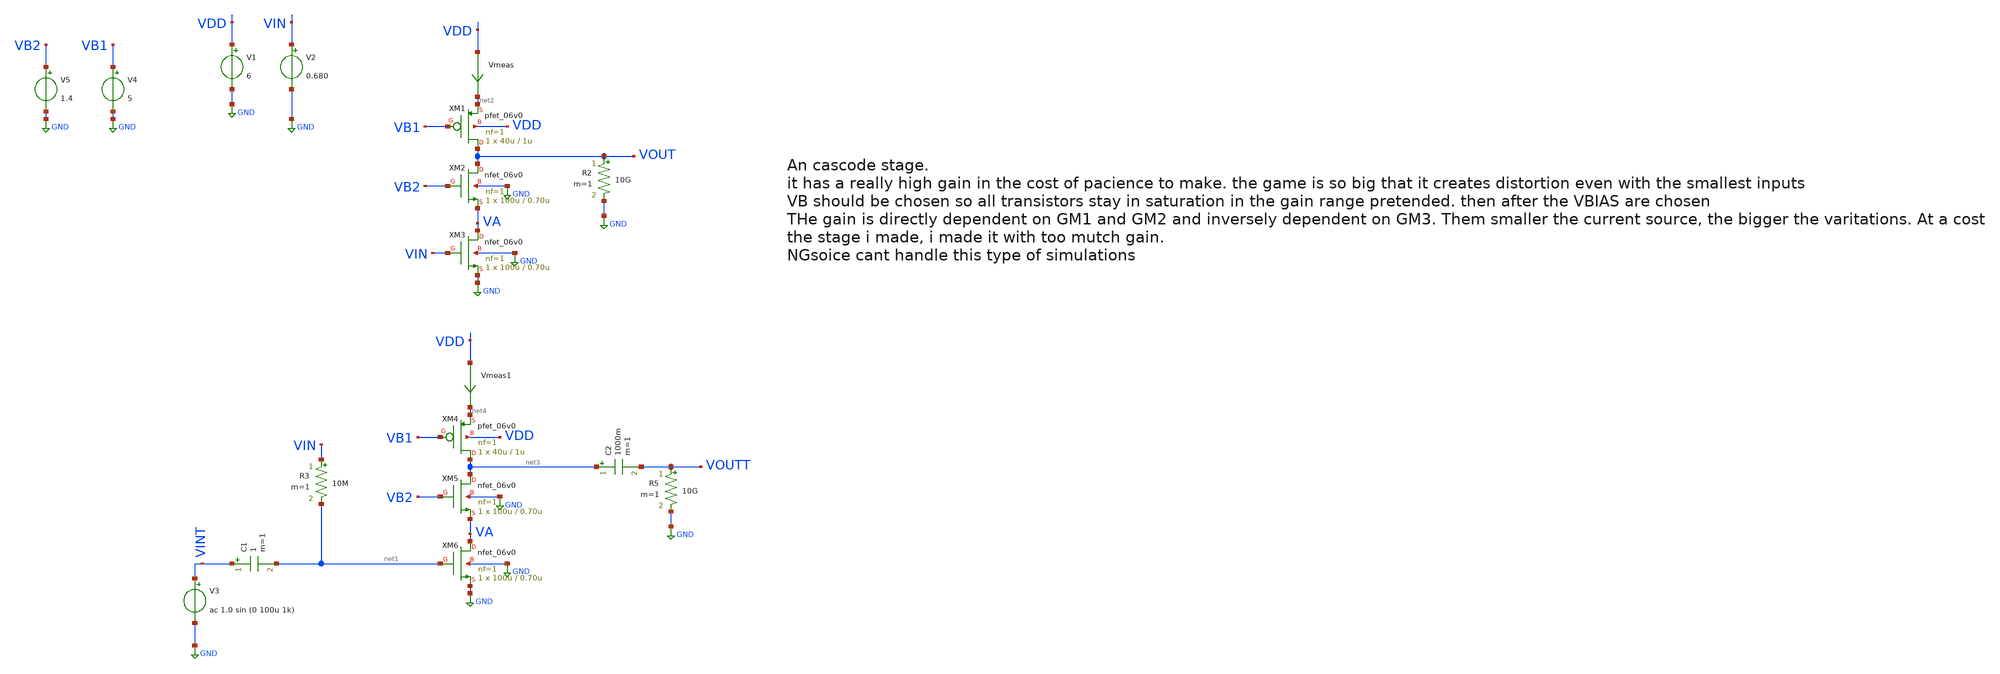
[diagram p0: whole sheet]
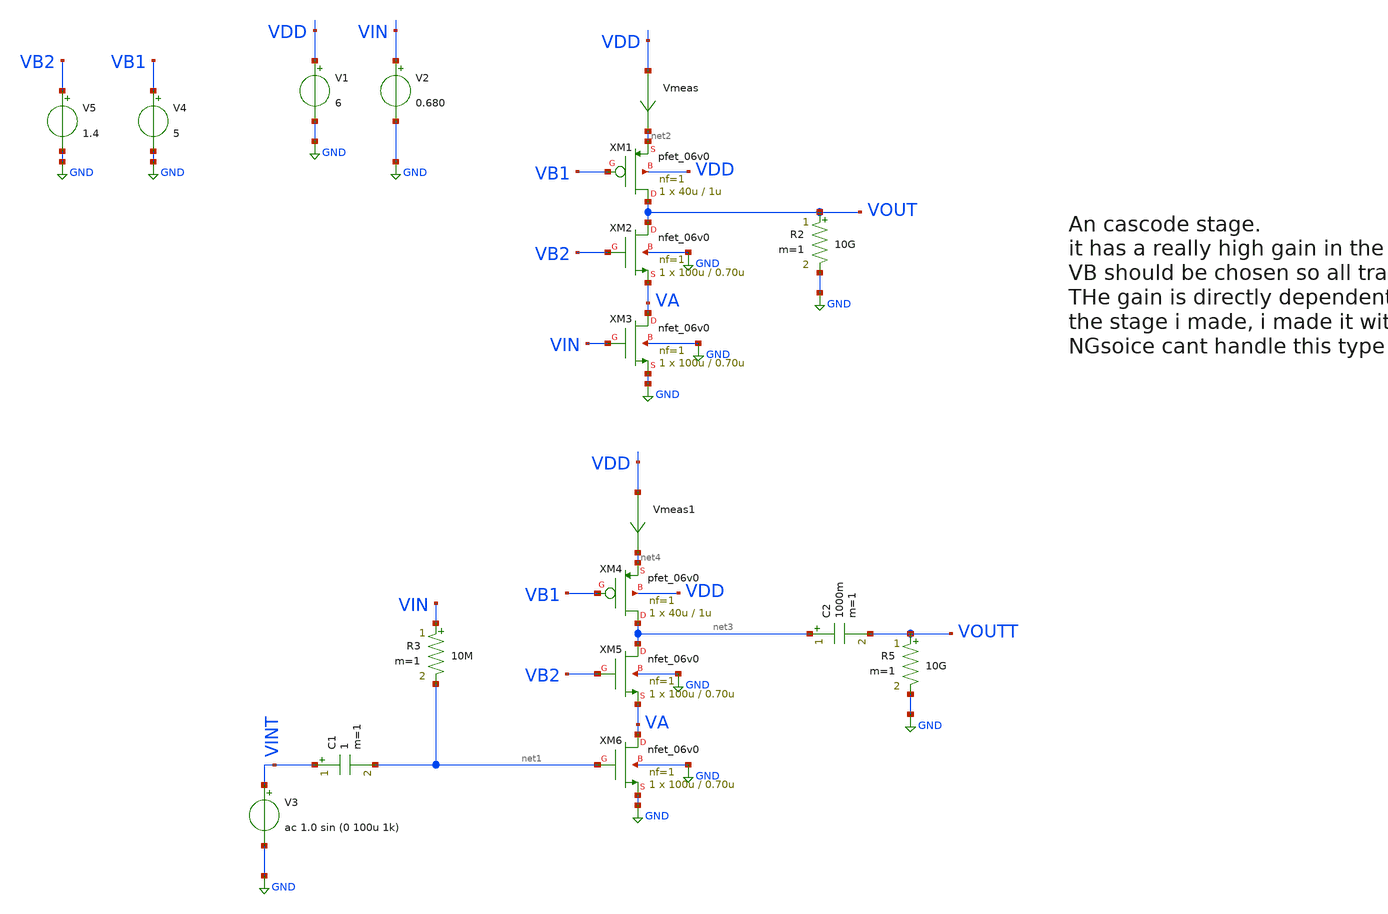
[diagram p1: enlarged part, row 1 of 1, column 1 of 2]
** sch_path: unusual_amplifiers/unusual_amp10.sch
**.subckt unusual_amp10
Vmeas VDD net2 0
.save i(vmeas)
V1 VDD GND 6
V2 VIN GND 0.680
V3 VINT GND ac 1.0 sin (0 100u 1k)
R2 VOUT GND 10G m=1
C1 VINT net1 1 m=1
R3 VIN net1 10M m=1
C2 net3 VOUTT 1000m m=1
R5 VOUTT GND 10G m=1
V4 VB1 GND 5
XM1 VOUT VB1 net2 VDD pfet_06v0 L=1u W=40u nf=1 ad='int((nf+1)/2) * W/nf * 0.18u' as='int((nf+2)/2) * W/nf * 0.18u'
+ pd='2*int((nf+1)/2) * (W/nf + 0.18u)' ps='2*int((nf+2)/2) * (W/nf + 0.18u)' nrd='0.18u / W' nrs='0.18u / W'
+ sa=0 sb=0 sd=0 m=1
XM2 VOUT VB2 VA GND nfet_06v0 L=0.70u W=100u nf=1 ad='int((nf+1)/2) * W/nf * 0.18u' as='int((nf+2)/2) * W/nf * 0.18u'
+ pd='2*int((nf+1)/2) * (W/nf + 0.18u)' ps='2*int((nf+2)/2) * (W/nf + 0.18u)' nrd='0.18u / W' nrs='0.18u / W'
+ sa=0 sb=0 sd=0 m=1
XM3 VA VIN GND GND nfet_06v0 L=0.70u W=100u nf=1 ad='int((nf+1)/2) * W/nf * 0.18u' as='int((nf+2)/2) * W/nf * 0.18u'
+ pd='2*int((nf+1)/2) * (W/nf + 0.18u)' ps='2*int((nf+2)/2) * (W/nf + 0.18u)' nrd='0.18u / W' nrs='0.18u / W'
+ sa=0 sb=0 sd=0 m=1
V5 VB2 GND 1.4
Vmeas1 VDD net4 0
.save i(vmeas1)
XM4 net3 VB1 net4 VDD pfet_06v0 L=1u W=40u nf=1 ad='int((nf+1)/2) * W/nf * 0.18u' as='int((nf+2)/2) * W/nf * 0.18u'
+ pd='2*int((nf+1)/2) * (W/nf + 0.18u)' ps='2*int((nf+2)/2) * (W/nf + 0.18u)' nrd='0.18u / W' nrs='0.18u / W'
+ sa=0 sb=0 sd=0 m=1
XM5 net3 VB2 VA GND nfet_06v0 L=0.70u W=100u nf=1 ad='int((nf+1)/2) * W/nf * 0.18u' as='int((nf+2)/2) * W/nf * 0.18u'
+ pd='2*int((nf+1)/2) * (W/nf + 0.18u)' ps='2*int((nf+2)/2) * (W/nf + 0.18u)' nrd='0.18u / W' nrs='0.18u / W'
+ sa=0 sb=0 sd=0 m=1
XM6 VA net1 GND GND nfet_06v0 L=0.70u W=100u nf=1 ad='int((nf+1)/2) * W/nf * 0.18u' as='int((nf+2)/2) * W/nf * 0.18u'
+ pd='2*int((nf+1)/2) * (W/nf + 0.18u)' ps='2*int((nf+2)/2) * (W/nf + 0.18u)' nrd='0.18u / W' nrs='0.18u / W'
+ sa=0 sb=0 sd=0 m=1
**** begin user architecture code

**************************************************************
**************************************************************
**************************************************************
**************************************************************
**************************************************************
*LIBs*********************************************************
**************************************************************
**************************************************************
**************************************************************
**************************************************************
**************************************************************
.include $::180MCU_MODELS/design.ngspice
*.lib $::180MCU_MODELS/sm141064.ngspice statistical *use statistical if you want global and parameter mismatch
*.lib $::180MCU_MODELS/sm141064.ngspice res_statistical
.lib $::180MCU_MODELS/sm141064.ngspice typical
.lib $::180MCU_MODELS/sm141064.ngspice res_typical
.lib $::180MCU_MODELS/sm141064.ngspice moscap_typical
.lib $::180MCU_MODELS/sm141064.ngspice bjt_typical
.lib $::180MCU_MODELS/sm141064.ngspice diode_typical
.lib $::180MCU_MODELS/sm141064.ngspice mimcap_typical
**************************************************************
**************************************************************
**************************************************************
**************************************************************
**************************************************************
*Corners/montecarlo options***********************************
**************************************************************
**************************************************************
**************************************************************
**************************************************************
**************************************************************
.TEMP 27
.param   sw_stat_global = 1   sw_stat_mism = 1  mc_skew = 3  res_mc_skew = 3  cap_mc_skew = 3
+  fnoicor = 1
**************************************************************
**************************************************************
**************************************************************
**************************************************************
*SIMULATION and Plots*****************************************
**************************************************************
**************************************************************
**************************************************************
**************************************************************
.control
save all
dc V2 0 6 0.01
*dc simulation
plot v(VOUT) v(VIN) deriv(v(VOUT)) v(VA)
plot v(VA)
*ploting VIN VOUT and the voltage gain
plot i(Vmeas)
*ploting the current for curiosity
tran 1us 2m
*transient simulation
plot (v(VINT)) (v(VOUTT))
*simple plot to exemplify the gain
fft v(VOUTT) v(VINT)
*fast fourier transfor
plot mag(v(VOUTT)) mag(v(VINT))
* analyse the frequency spectrum of the transient waves, to detect distortion
ac dec 20 1 50G
*simple ac simulation
plot v(VOUTT)
*gain in function of the input frequency
.endc

**** end user architecture code
**.ends
.GLOBAL GND
.end
